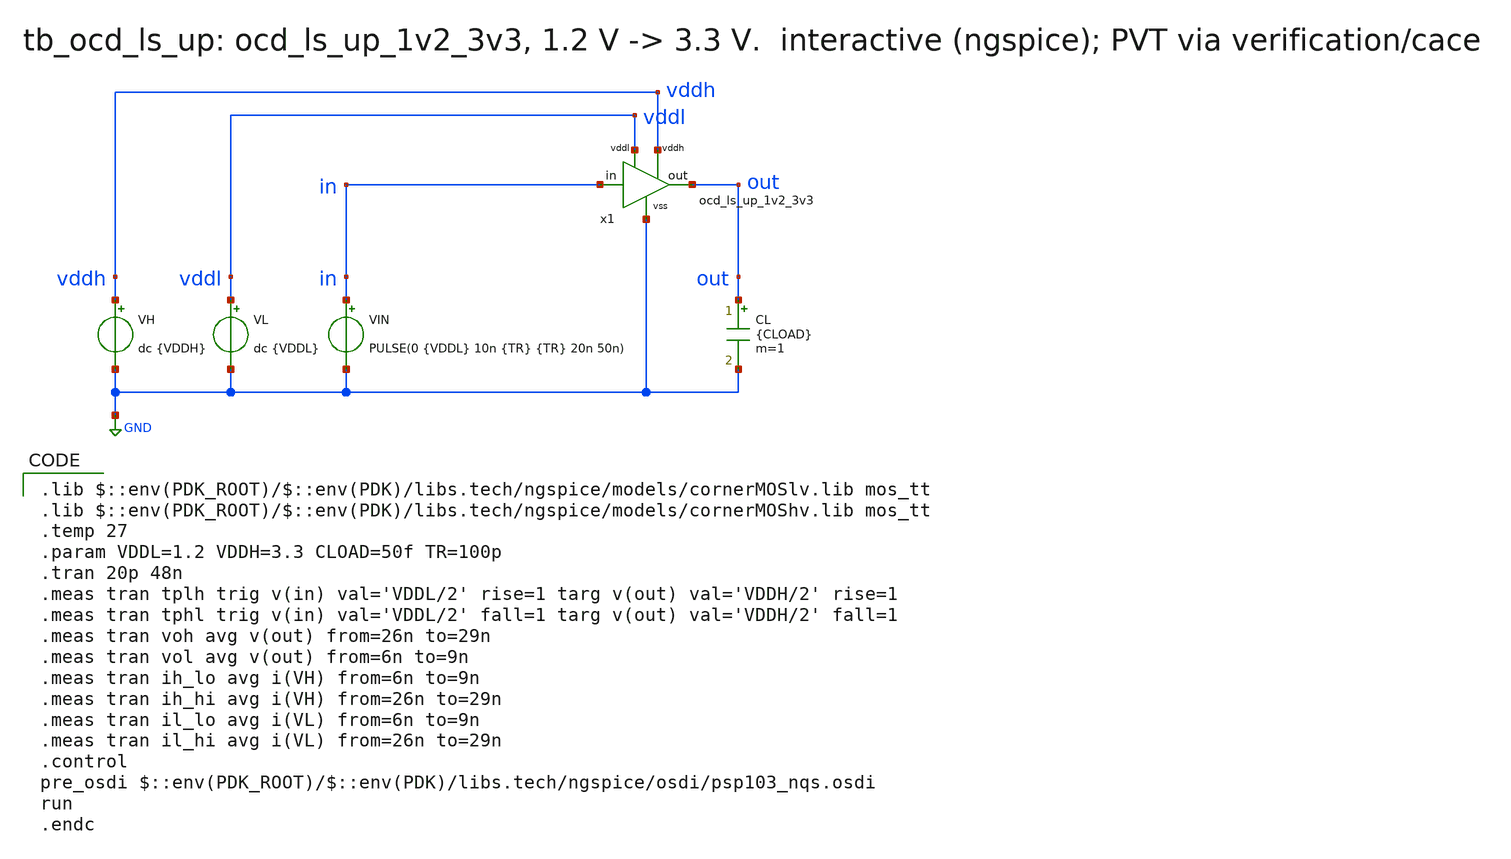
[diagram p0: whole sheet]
** sch_path: macros/ocd_ls_up_1v2_3v3/testbenches/xschem/tb_ocd_ls_up.sch
* macros/ocd_ls_up_1v2_3v3/schematic/xschem/ocd_ls_up_1v2_3v3.sym:
* Copyright 2023 IHP PDK Authors, Apache License 2.0 (https://www.apache.org/licenses/LICENSE-2.0)
**.subckt tb_ocd_ls_up
x1 GND vddl vddh out in ocd_ls_up_1v2_3v3
VL vddl GND dc {VDDL}
VH vddh GND dc {VDDH}
VIN in GND PULSE(0 {VDDL} 10n {TR} {TR} 20n 50n)
CL out GND {CLOAD} m=1
**** begin user architecture code
 .lib $::env(PDK_ROOT)/$::env(PDK)/libs.tech/ngspice/models/cornerMOSlv.lib mos_tt
.lib $::env(PDK_ROOT)/$::env(PDK)/libs.tech/ngspice/models/cornerMOShv.lib mos_tt
.temp 27
.param VDDL=1.2 VDDH=3.3 CLOAD=50f TR=100p
.tran 20p 48n
.meas tran tplh trig v(in) val='VDDL/2' rise=1 targ v(out) val='VDDH/2' rise=1
.meas tran tphl trig v(in) val='VDDL/2' fall=1 targ v(out) val='VDDH/2' fall=1
.meas tran voh avg v(out) from=26n to=29n
.meas tran vol avg v(out) from=6n to=9n
.meas tran ih_lo avg i(VH) from=6n to=9n
.meas tran ih_hi avg i(VH) from=26n to=29n
.meas tran il_lo avg i(VL) from=6n to=9n
.meas tran il_hi avg i(VL) from=26n to=29n
.control
pre_osdi $::env(PDK_ROOT)/$::env(PDK)/libs.tech/ngspice/osdi/psp103_nqs.osdi
run
.endc
**** end user architecture code
**.ends

* expanding   symbol:  ocd_ls_up_1v2_3v3.sym # of pins=5
** sym_path: macros/ocd_ls_up_1v2_3v3/schematic/xschem/ocd_ls_up_1v2_3v3.sym
** sch_path: macros/ocd_ls_up_1v2_3v3/schematic/xschem/ocd_ls_up_1v2_3v3.sch
.subckt ocd_ls_up_1v2_3v3 vss vddl vddh out in
*.iopin vss
*.iopin vddl
*.iopin vddh
*.opin out
*.ipin in
x2 net1 in vddl vss sg13cmos5l_inv_4
x3 net2 net1 vddl vss sg13cmos5l_inv_4
x1 net2 net1 out net3 vddh vss sw_lvl_shift
.ends


* expanding   symbol:  sw_lvl_shift.sym # of pins=4
** sym_path: macros/ocd_analog_switches/schematic/xschem/sw_lvl_shift.sym
** sch_path: macros/ocd_analog_switches/schematic/xschem/sw_lvl_shift.sch
.subckt sw_lvl_shift in_p in_n out outn avdd avss
*.ipin in_n
*.ipin in_p
*.opin out
*.opin outn
XM1 net1 in_p avss avss sg13_hv_nmos w=2u l=0.5u ng=1 m=1 mm_ok=1
XM2 net1 S1_N avdd avdd sg13_hv_pmos w=0.5u l=0.5u ng=1 m=1 mm_ok=1
XM3 S1_N in_n avss avss sg13_hv_nmos w=2u l=0.5u ng=1 m=1 mm_ok=1
XM4 S1_N net1 avdd avdd sg13_hv_pmos w=0.5u l=0.5u ng=1 m=1 mm_ok=1
XM5 outn S1_N avdd avdd sg13_hv_pmos w=2u l=0.5u ng=1 m=2 mm_ok=1
XM6 outn S1_N avss avss sg13_hv_nmos w=1u l=0.5u ng=1 m=2 mm_ok=1
XM7 out outn avdd avdd sg13_hv_pmos w=2u l=0.5u ng=1 m=2 mm_ok=1
XM8 out outn avss avss sg13_hv_nmos w=1u l=0.5u ng=1 m=2 mm_ok=1
.ends

.GLOBAL GND
.end
